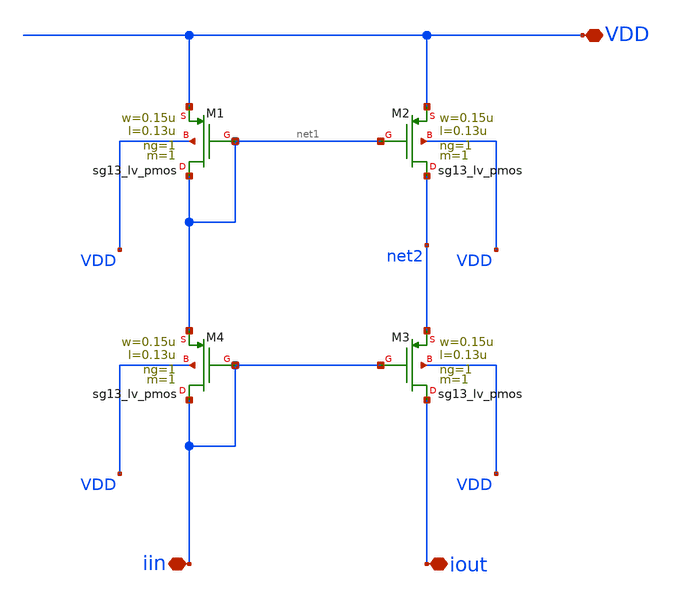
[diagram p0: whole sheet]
** sch_path: analog-db/templates/current_mirror/pmos_current_source/cascode_current_mirror.sch
* Copyright 2026 MacAnalog Research Group
**.subckt cascode_current_mirror iout VDD iin
*.iopin iout
*.iopin VDD
*.iopin iin
XM1 net1 net1 VDD VDD sg13_lv_pmos w=0.15u l=0.13u ng=1 m=1 mm_ok=1
XM2 net2 net1 VDD VDD sg13_lv_pmos w=0.15u l=0.13u ng=1 m=1 mm_ok=1
XM3 iout iin net2 VDD sg13_lv_pmos w=0.15u l=0.13u ng=1 m=1 mm_ok=1
XM4 iin iin net1 VDD sg13_lv_pmos w=0.15u l=0.13u ng=1 m=1 mm_ok=1
**.ends
.end
